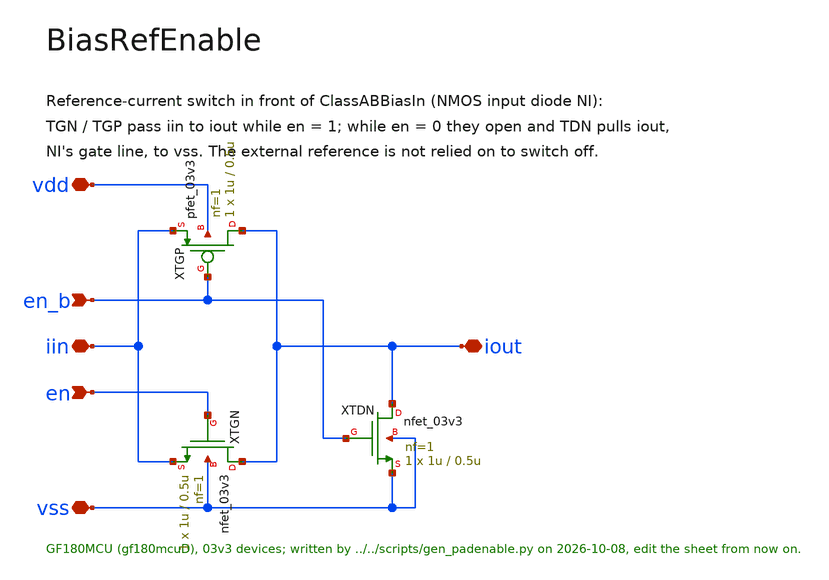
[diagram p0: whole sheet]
** sch_path: macros/PadEnable/schematic/xschem/BiasRefEnable.sch
**.subckt BiasRefEnable vdd vss en en_b iin iout
*.iopin vdd
*.iopin vss
*.ipin en
*.ipin en_b
*.iopin iin
*.iopin iout
XTGP iout en_b iin vdd pfet_03v3 L=0.5u W=1u nf=1 ad='int((nf+1)/2) * W/nf * 0.18u' as='int((nf+2)/2) * W/nf * 0.18u'
+ pd='2*int((nf+1)/2) * (W/nf + 0.18u)' ps='2*int((nf+2)/2) * (W/nf + 0.18u)' nrd='0.18u / W' nrs='0.18u / W'
+ sa=0 sb=0 sd=0 m=1
XTGN iout en iin vss nfet_03v3 L=0.5u W=1u nf=1 ad='int((nf+1)/2) * W/nf * 0.18u' as='int((nf+2)/2) * W/nf * 0.18u'
+ pd='2*int((nf+1)/2) * (W/nf + 0.18u)' ps='2*int((nf+2)/2) * (W/nf + 0.18u)' nrd='0.18u / W' nrs='0.18u / W'
+ sa=0 sb=0 sd=0 m=1
XTDN iout en_b vss vss nfet_03v3 L=0.5u W=1u nf=1 ad='int((nf+1)/2) * W/nf * 0.18u' as='int((nf+2)/2) * W/nf * 0.18u'
+ pd='2*int((nf+1)/2) * (W/nf + 0.18u)' ps='2*int((nf+2)/2) * (W/nf + 0.18u)' nrd='0.18u / W' nrs='0.18u / W'
+ sa=0 sb=0 sd=0 m=1
**.ends
.end
